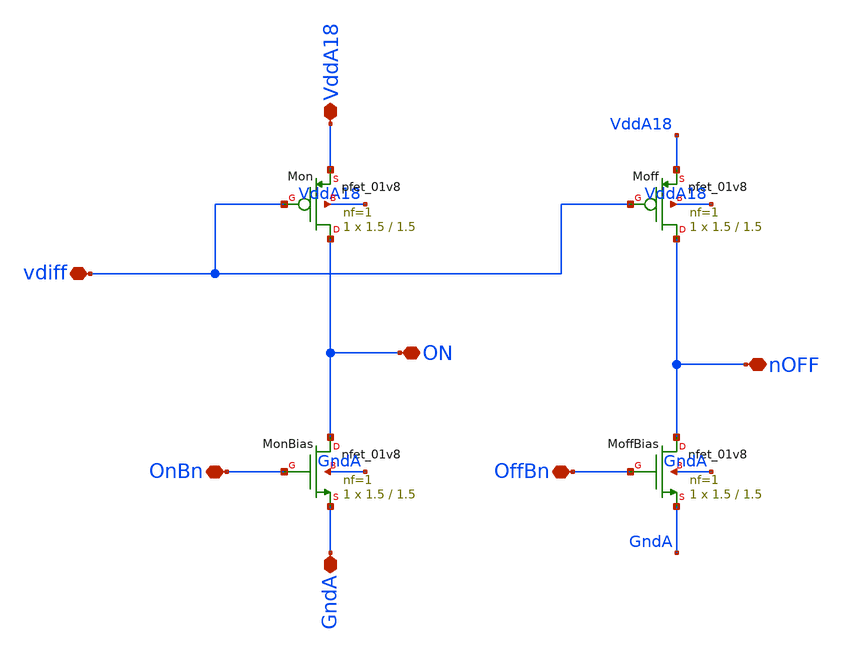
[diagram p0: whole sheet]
** sch_path: analog/klayout/production/final_merge_20260923/testbenches/cace/analog/xschem/PixelComparators.sch
**.subckt PixelComparators OnBn OffBn VddA18 vdiff GndA ON nOFF
*.iopin OnBn
*.iopin OffBn
*.iopin VddA18
*.iopin vdiff
*.iopin GndA
*.iopin ON
*.iopin nOFF
XMonBias ON OnBn GndA GndA sky130_fd_pr__nfet_01v8 L=1.5 W=1.5 nf=1 ad='int((1 + 1)/2) * 1.5 / 1 * 0.29'
+ as='int((1 + 2)/2) * 1.5 / 1 * 0.29' pd='2*int((1 + 1)/2) * (1.5 / 1 + 0.29)' ps='2*int((1 + 2)/2) * (1.5 / 1 + 0.29)'
+ nrd='0.29 / 1.5 ' nrs='0.29 / 1.5 ' sa=0 sb=0 sd=0 mult=1 m=1
XMoffBias nOFF OffBn GndA GndA sky130_fd_pr__nfet_01v8 L=1.5 W=1.5 nf=1 ad='int((1 + 1)/2) * 1.5 / 1 * 0.29'
+ as='int((1 + 2)/2) * 1.5 / 1 * 0.29' pd='2*int((1 + 1)/2) * (1.5 / 1 + 0.29)' ps='2*int((1 + 2)/2) * (1.5 / 1 + 0.29)'
+ nrd='0.29 / 1.5 ' nrs='0.29 / 1.5 ' sa=0 sb=0 sd=0 mult=1 m=1
XMon ON vdiff VddA18 VddA18 sky130_fd_pr__pfet_01v8 L=1.5 W=1.5 nf=1 ad='int((1 + 1)/2) * 1.5 / 1 * 0.29'
+ as='int((1 + 2)/2) * 1.5 / 1 * 0.29' pd='2*int((1 + 1)/2) * (1.5 / 1 + 0.29)' ps='2*int((1 + 2)/2) * (1.5 / 1 + 0.29)'
+ nrd='0.29 / 1.5 ' nrs='0.29 / 1.5 ' sa=0 sb=0 sd=0 mult=1 m=1
XMoff nOFF vdiff VddA18 VddA18 sky130_fd_pr__pfet_01v8 L=1.5 W=1.5 nf=1 ad='int((1 + 1)/2) * 1.5 / 1 * 0.29'
+ as='int((1 + 2)/2) * 1.5 / 1 * 0.29' pd='2*int((1 + 1)/2) * (1.5 / 1 + 0.29)' ps='2*int((1 + 2)/2) * (1.5 / 1 + 0.29)'
+ nrd='0.29 / 1.5 ' nrs='0.29 / 1.5 ' sa=0 sb=0 sd=0 mult=1 m=1
**.ends
.end
